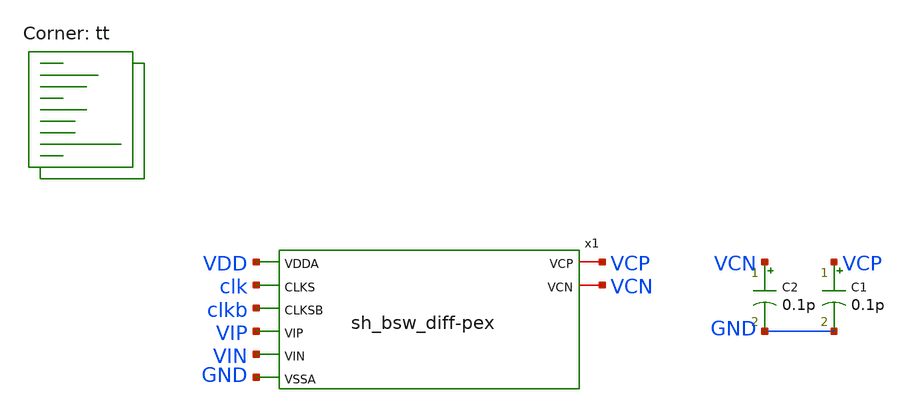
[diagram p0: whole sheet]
** sch_path: xschem/sh_bsw_diff-PEX-tb.sch
**.subckt sh_bsw_diff-PEX-tb
C1 VCP GND 0.1p m=1
C2 VCN GND 0.1p m=1
x1 VDD clk clkb VIP VIN GND VCP VCN sh_bsw_diff-pex
**** begin user architecture code
 .lib $::SKYWATER_MODELS/sky130.lib.spice tt
.include $::SKYWATER_STDCELLS/sky130_fd_sc_hd.spice
.param mc_mm_switch = 0
.param mc_pr_switch = 0




   .include ~/sky130_projects/UNIC-CASS-2024/spice/sh_bsw4-pex.spice
  .param fin=9.3e3 in_delay={10e-9} in_period={1/fin} vcn_delay={in_period/2}
  .param fclk={20e3} tclk={1/fclk} thclk={tclk/2}
  .option wnflag=1
  .option safecurrents

  Vvdd   vdd   gnd 1.8
  Vdtp   vip   gnd sin(0.5 0.5 {fin} {in_delay})
  Vdtn   vin   gnd sin(0.5 0.5 {fin} {in_delay+vcn_delay})
  Vclk   clk   gnd pulse(0 1.8 10e-9 1p 1p {thclk} {tclk})
  Vclkb  clkb  gnd pulse(1.8 0 10e-9 1p 1p {thclk} {tclk})

  .control
     reset
     save all
     tran 10n 1m uic
     write sh_bsw_diff-PEX-tb.raw
    quit 0
  .endc



**** end user architecture code
**.ends
.end
